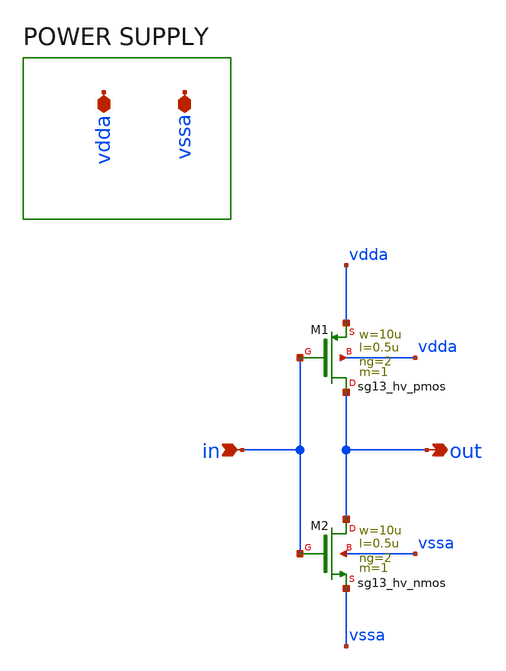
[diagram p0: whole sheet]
** sch_path: inv_hc.sch
**.subckt inv_hc in out vssa vdda
*.ipin in
*.opin out
*.iopin vssa
*.iopin vdda
XM1 out in vdda vdda sg13_hv_pmos w=10u l=0.5u ng=2 m=1 mm_ok=1
XM2 out in vssa vssa sg13_hv_nmos w=10u l=0.5u ng=2 m=1 mm_ok=1
**.ends
.end
